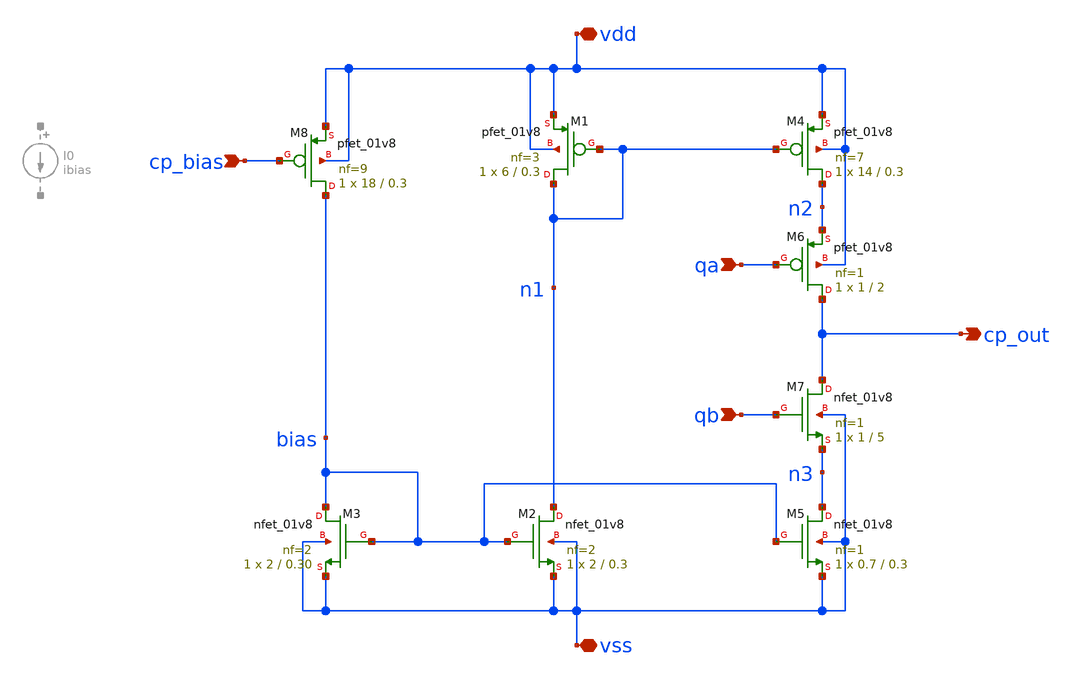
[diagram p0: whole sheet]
** sch_path: xschem/PLL_FOLDER/cp/cp_schem.sch
**.subckt cp_schem qa qb cp_out vdd vss cp_bias
*.ipin qa
*.ipin qb
*.opin cp_out
*.iopin vdd
*.iopin vss
*.ipin cp_bias
XM1 n1 n1 vdd vdd sky130_fd_pr__pfet_01v8 L=0.3 W=6 nf=3 ad='int((nf+1)/2) * W/nf * 0.29' as='int((nf+2)/2) * W/nf * 0.29'
+ pd='2*int((nf+1)/2) * (W/nf + 0.29)' ps='2*int((nf+2)/2) * (W/nf + 0.29)' nrd='0.29 / W' nrs='0.29 / W'
+ sa=0 sb=0 sd=0 mult=1 m=1
XM2 n1 bias vss vss sky130_fd_pr__nfet_01v8 L=0.3 W=2 nf=2 ad='int((nf+1)/2) * W/nf * 0.29' as='int((nf+2)/2) * W/nf * 0.29'
+ pd='2*int((nf+1)/2) * (W/nf + 0.29)' ps='2*int((nf+2)/2) * (W/nf + 0.29)' nrd='0.29 / W' nrs='0.29 / W'
+ sa=0 sb=0 sd=0 mult=1 m=1
XM3 bias bias vss vss sky130_fd_pr__nfet_01v8 L=0.30 W=2 nf=2 ad='int((nf+1)/2) * W/nf * 0.29' as='int((nf+2)/2) * W/nf * 0.29'
+ pd='2*int((nf+1)/2) * (W/nf + 0.29)' ps='2*int((nf+2)/2) * (W/nf + 0.29)' nrd='0.29 / W' nrs='0.29 / W'
+ sa=0 sb=0 sd=0 mult=1 m=1
XM4 n2 n1 vdd vdd sky130_fd_pr__pfet_01v8 L=0.3 W=14 nf=7 ad='int((nf+1)/2) * W/nf * 0.29' as='int((nf+2)/2) * W/nf * 0.29'
+ pd='2*int((nf+1)/2) * (W/nf + 0.29)' ps='2*int((nf+2)/2) * (W/nf + 0.29)' nrd='0.29 / W' nrs='0.29 / W'
+ sa=0 sb=0 sd=0 mult=1 m=1
XM5 n3 bias vss vss sky130_fd_pr__nfet_01v8 L=0.3 W=0.7 nf=1 ad='int((nf+1)/2) * W/nf * 0.29' as='int((nf+2)/2) * W/nf * 0.29'
+ pd='2*int((nf+1)/2) * (W/nf + 0.29)' ps='2*int((nf+2)/2) * (W/nf + 0.29)' nrd='0.29 / W' nrs='0.29 / W'
+ sa=0 sb=0 sd=0 mult=1 m=1
XM6 cp_out qa n2 vdd sky130_fd_pr__pfet_01v8 L=2 W=1 nf=1 ad='int((nf+1)/2) * W/nf * 0.29' as='int((nf+2)/2) * W/nf * 0.29'
+ pd='2*int((nf+1)/2) * (W/nf + 0.29)' ps='2*int((nf+2)/2) * (W/nf + 0.29)' nrd='0.29 / W' nrs='0.29 / W'
+ sa=0 sb=0 sd=0 mult=1 m=1
XM7 cp_out qb n3 vss sky130_fd_pr__nfet_01v8 L=5 W=1 nf=1 ad='int((nf+1)/2) * W/nf * 0.29' as='int((nf+2)/2) * W/nf * 0.29'
+ pd='2*int((nf+1)/2) * (W/nf + 0.29)' ps='2*int((nf+2)/2) * (W/nf + 0.29)' nrd='0.29 / W' nrs='0.29 / W'
+ sa=0 sb=0 sd=0 mult=1 m=1
XM8 bias cp_bias vdd vdd sky130_fd_pr__pfet_01v8 L=0.3 W=18 nf=9 ad='int((nf+1)/2) * W/nf * 0.29' as='int((nf+2)/2) * W/nf * 0.29'
+ pd='2*int((nf+1)/2) * (W/nf + 0.29)' ps='2*int((nf+2)/2) * (W/nf + 0.29)' nrd='0.29 / W' nrs='0.29 / W'
+ sa=0 sb=0 sd=0 mult=1 m=1
**.ends
.end
